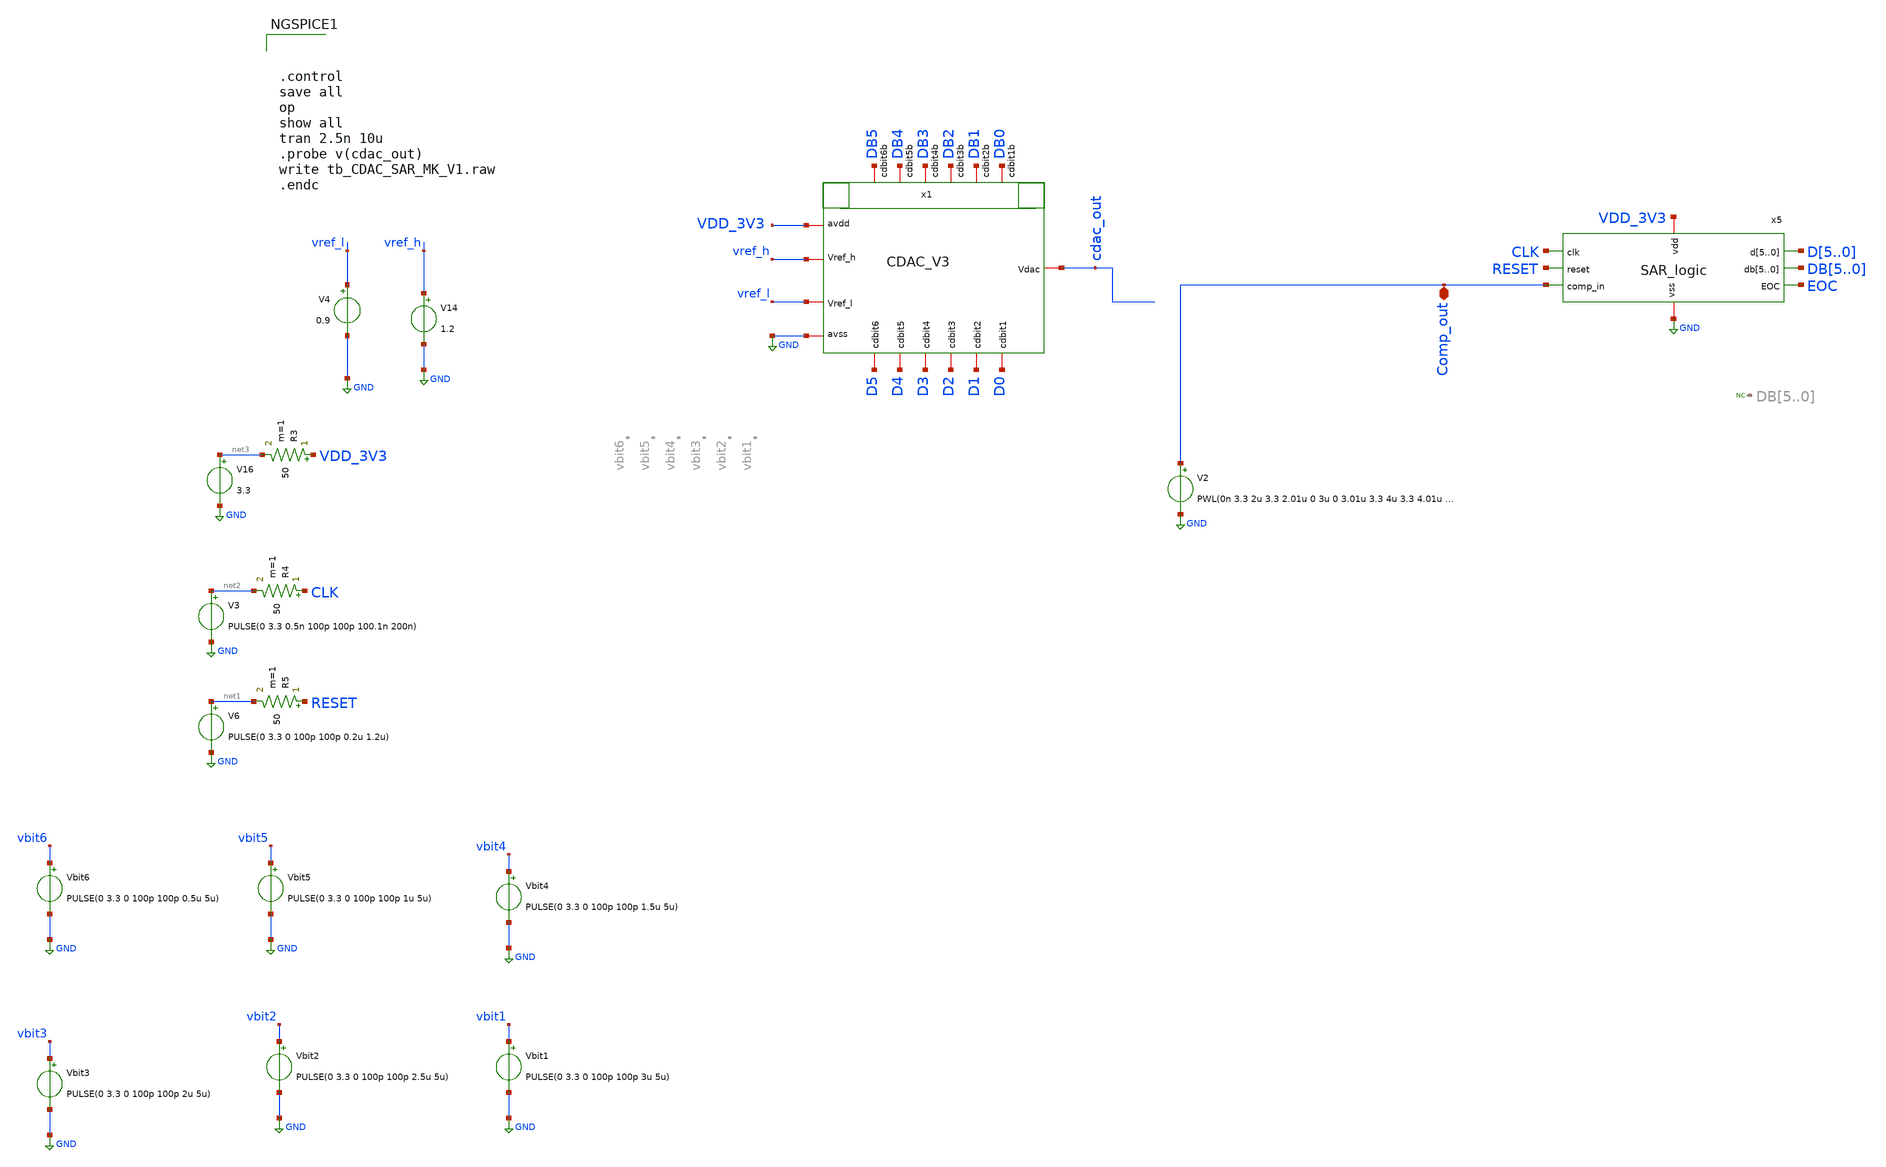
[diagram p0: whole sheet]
** sch_path: designs/full_ADC/TB_CDAC_SAR_MK_V1.sch
**.subckt TB_CDAC_SAR_MK_V1 Comp_out
*.iopin Comp_out
V14 vref_h GND 1.2
V6 net1 GND PULSE(0 3.3 0 100p 100p 0.2u 1.2u)
R5 RESET net1 50 m=1
x5 VDD_3V3 GND CLK RESET Comp_out D5 D4 D3 D2 D1 D0 DB5 DB4 DB3 DB2 DB1 DB0 EOC SAR_logic
V3 net2 GND PULSE(0 3.3 0.5n 100p 100p 100.1n 200n)
R4 CLK net2 50 m=1
V4 vref_l GND 0.9
V16 net3 GND 3.3
R3 VDD_3V3 net3 50 m=1
V2 Comp_out GND PWL(0n 3.3 2u 3.3 2.01u 0 3u 0 3.01u 3.3 4u 3.3 4.01u 0 6u 0 6.01u 3.3
Vbit1 vbit1 GND PULSE(0 3.3 0 100p 100p 3u 5u)
Vbit2 vbit2 GND PULSE(0 3.3 0 100p 100p 2.5u 5u)
Vbit3 vbit3 GND PULSE(0 3.3 0 100p 100p 2u 5u)
Vbit4 vbit4 GND PULSE(0 3.3 0 100p 100p 1.5u 5u)
Vbit5 vbit5 GND PULSE(0 3.3 0 100p 100p 1u 5u)
Vbit6 vbit6 GND PULSE(0 3.3 0 100p 100p 0.5u 5u)
x1 DB5 DB2 DB4 DB0 DB1 DB3 vref_l cdac_out VDD_3V3 GND vref_h D5 D4 D2 D0 D1 D3 CDAC_V3
**** begin user architecture code



.control
save all
op
show all
tran 2.5n 10u
.probe v(cdac_out)
write tb_CDAC_SAR_MK_V1.raw
.endc



.include $::180MCU_MODELS/design.ngspice
.lib $::180MCU_MODELS/sm141064.ngspice typical
.lib $::180MCU_MODELS/sm141064.ngspice cap_mim
.lib $::180MCU_MODELS/sm141064.ngspice res_typical
.lib $::180MCU_MODELS/sm141064.ngspice moscap_typical
.lib $::180MCU_MODELS/sm141064.ngspice mimcap_typical
* .lib $::180MCU_MODELS/sm141064.ngspice res_statistical

**** end user architecture code
**.ends
.GLOBAL GND
.end
